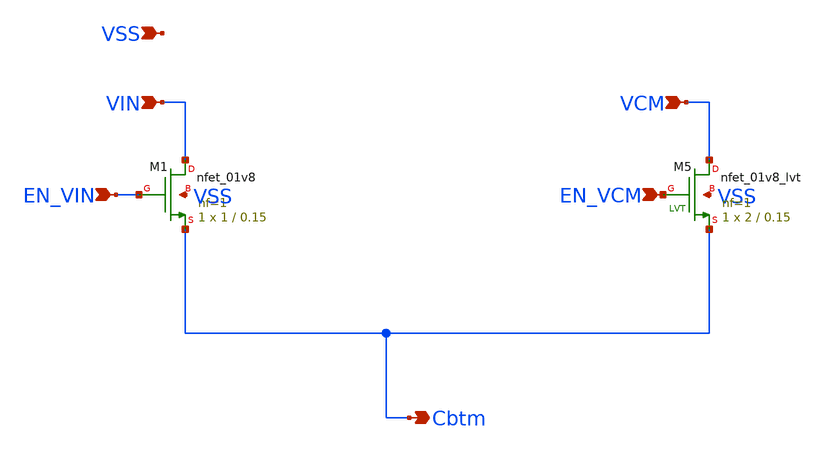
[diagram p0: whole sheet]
** sch_path: individual_switches/switch_C0_dummy.sch
**.subckt switch_C0_dummy VIN EN_VIN VCM EN_VCM Cbtm VSS
*.ipin VIN
*.ipin EN_VIN
*.ipin VCM
*.ipin EN_VCM
*.opin Cbtm
*.ipin VSS
XM1 VIN EN_VIN Cbtm VSS sky130_fd_pr__nfet_01v8 L=0.15 W=1 nf=1 ad='int((nf+1)/2) * W/nf * 0.29' as='int((nf+2)/2) * W/nf * 0.29'
+ pd='2*int((nf+1)/2) * (W/nf + 0.29)' ps='2*int((nf+2)/2) * (W/nf + 0.29)' nrd='0.29 / W' nrs='0.29 / W'
+ sa=0 sb=0 sd=0 mult=1 m=1
XM5 VCM EN_VCM Cbtm VSS sky130_fd_pr__nfet_01v8_lvt L=0.15 W=2 nf=1 ad='int((nf+1)/2) * W/nf * 0.29'
+ as='int((nf+2)/2) * W/nf * 0.29' pd='2*int((nf+1)/2) * (W/nf + 0.29)' ps='2*int((nf+2)/2) * (W/nf + 0.29)'
+ nrd='0.29 / W' nrs='0.29 / W' sa=0 sb=0 sd=0 mult=1 m=1
**.ends
.end
